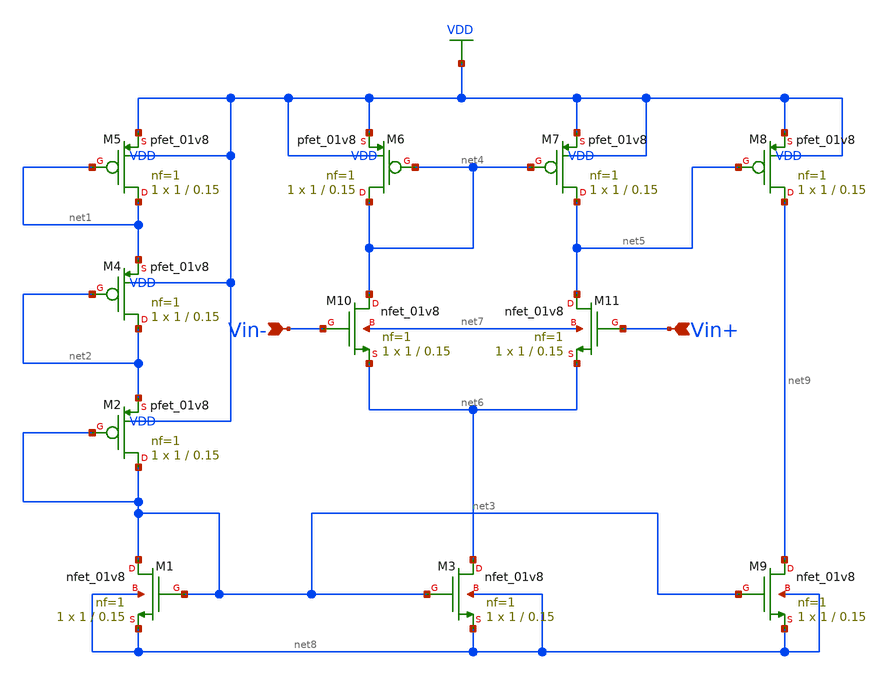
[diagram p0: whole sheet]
** sch_path: xschem/untitled.sch
**.subckt untitled Vin- Vin+
*.ipin Vin-
*.ipin Vin+
XM1 net3 net3 net8 net8 sky130_fd_pr__nfet_01v8 L=0.15 W=1 nf=1 ad='int((1 + 1)/2) * 1 / 1 * 0.29' as='int((1 + 2)/2) * 1 / 1 * 0.29'
+ pd='2*int((1 + 1)/2) * (1 / 1 + 0.29)' ps='2*int((1 + 2)/2) * (1 / 1 + 0.29)' nrd='0.29 / 1 ' nrs='0.29 / 1 '
+ sa=0 sb=0 sd=0 mult=1 m=1
XM2 net3 net3 net2 VDD sky130_fd_pr__pfet_01v8 L=0.15 W=1 nf=1 ad='int((1 + 1)/2) * 1 / 1 * 0.29' as='int((1 + 2)/2) * 1 / 1 * 0.29'
+ pd='2*int((1 + 1)/2) * (1 / 1 + 0.29)' ps='2*int((1 + 2)/2) * (1 / 1 + 0.29)' nrd='0.29 / 1 ' nrs='0.29 / 1 '
+ sa=0 sb=0 sd=0 mult=1 m=1
XM3 net6 net3 net8 net8 sky130_fd_pr__nfet_01v8 L=0.15 W=1 nf=1 ad='int((1 + 1)/2) * 1 / 1 * 0.29' as='int((1 + 2)/2) * 1 / 1 * 0.29'
+ pd='2*int((1 + 1)/2) * (1 / 1 + 0.29)' ps='2*int((1 + 2)/2) * (1 / 1 + 0.29)' nrd='0.29 / 1 ' nrs='0.29 / 1 '
+ sa=0 sb=0 sd=0 mult=1 m=1
XM4 net2 net2 net1 VDD sky130_fd_pr__pfet_01v8 L=0.15 W=1 nf=1 ad='int((1 + 1)/2) * 1 / 1 * 0.29' as='int((1 + 2)/2) * 1 / 1 * 0.29'
+ pd='2*int((1 + 1)/2) * (1 / 1 + 0.29)' ps='2*int((1 + 2)/2) * (1 / 1 + 0.29)' nrd='0.29 / 1 ' nrs='0.29 / 1 '
+ sa=0 sb=0 sd=0 mult=1 m=1
XM5 net1 net1 VDD VDD sky130_fd_pr__pfet_01v8 L=0.15 W=1 nf=1 ad='int((1 + 1)/2) * 1 / 1 * 0.29' as='int((1 + 2)/2) * 1 / 1 * 0.29'
+ pd='2*int((1 + 1)/2) * (1 / 1 + 0.29)' ps='2*int((1 + 2)/2) * (1 / 1 + 0.29)' nrd='0.29 / 1 ' nrs='0.29 / 1 '
+ sa=0 sb=0 sd=0 mult=1 m=1
XM6 net4 net4 VDD VDD sky130_fd_pr__pfet_01v8 L=0.15 W=1 nf=1 ad='int((1 + 1)/2) * 1 / 1 * 0.29' as='int((1 + 2)/2) * 1 / 1 * 0.29'
+ pd='2*int((1 + 1)/2) * (1 / 1 + 0.29)' ps='2*int((1 + 2)/2) * (1 / 1 + 0.29)' nrd='0.29 / 1 ' nrs='0.29 / 1 '
+ sa=0 sb=0 sd=0 mult=1 m=1
XM7 net5 net4 VDD VDD sky130_fd_pr__pfet_01v8 L=0.15 W=1 nf=1 ad='int((1 + 1)/2) * 1 / 1 * 0.29' as='int((1 + 2)/2) * 1 / 1 * 0.29'
+ pd='2*int((1 + 1)/2) * (1 / 1 + 0.29)' ps='2*int((1 + 2)/2) * (1 / 1 + 0.29)' nrd='0.29 / 1 ' nrs='0.29 / 1 '
+ sa=0 sb=0 sd=0 mult=1 m=1
XM8 net9 net5 VDD VDD sky130_fd_pr__pfet_01v8 L=0.15 W=1 nf=1 ad='int((1 + 1)/2) * 1 / 1 * 0.29' as='int((1 + 2)/2) * 1 / 1 * 0.29'
+ pd='2*int((1 + 1)/2) * (1 / 1 + 0.29)' ps='2*int((1 + 2)/2) * (1 / 1 + 0.29)' nrd='0.29 / 1 ' nrs='0.29 / 1 '
+ sa=0 sb=0 sd=0 mult=1 m=1
XM9 net9 net3 net8 net8 sky130_fd_pr__nfet_01v8 L=0.15 W=1 nf=1 ad='int((1 + 1)/2) * 1 / 1 * 0.29' as='int((1 + 2)/2) * 1 / 1 * 0.29'
+ pd='2*int((1 + 1)/2) * (1 / 1 + 0.29)' ps='2*int((1 + 2)/2) * (1 / 1 + 0.29)' nrd='0.29 / 1 ' nrs='0.29 / 1 '
+ sa=0 sb=0 sd=0 mult=1 m=1
XM10 net4 Vin- net6 net7 sky130_fd_pr__nfet_01v8 L=0.15 W=1 nf=1 ad='int((1 + 1)/2) * 1 / 1 * 0.29' as='int((1 + 2)/2) * 1 / 1 * 0.29'
+ pd='2*int((1 + 1)/2) * (1 / 1 + 0.29)' ps='2*int((1 + 2)/2) * (1 / 1 + 0.29)' nrd='0.29 / 1 ' nrs='0.29 / 1 '
+ sa=0 sb=0 sd=0 mult=1 m=1
XM11 net5 Vin+ net6 net7 sky130_fd_pr__nfet_01v8 L=0.15 W=1 nf=1 ad='int((1 + 1)/2) * 1 / 1 * 0.29' as='int((1 + 2)/2) * 1 / 1 * 0.29'
+ pd='2*int((1 + 1)/2) * (1 / 1 + 0.29)' ps='2*int((1 + 2)/2) * (1 / 1 + 0.29)' nrd='0.29 / 1 ' nrs='0.29 / 1 '
+ sa=0 sb=0 sd=0 mult=1 m=1
**.ends
.GLOBAL VDD
.end
